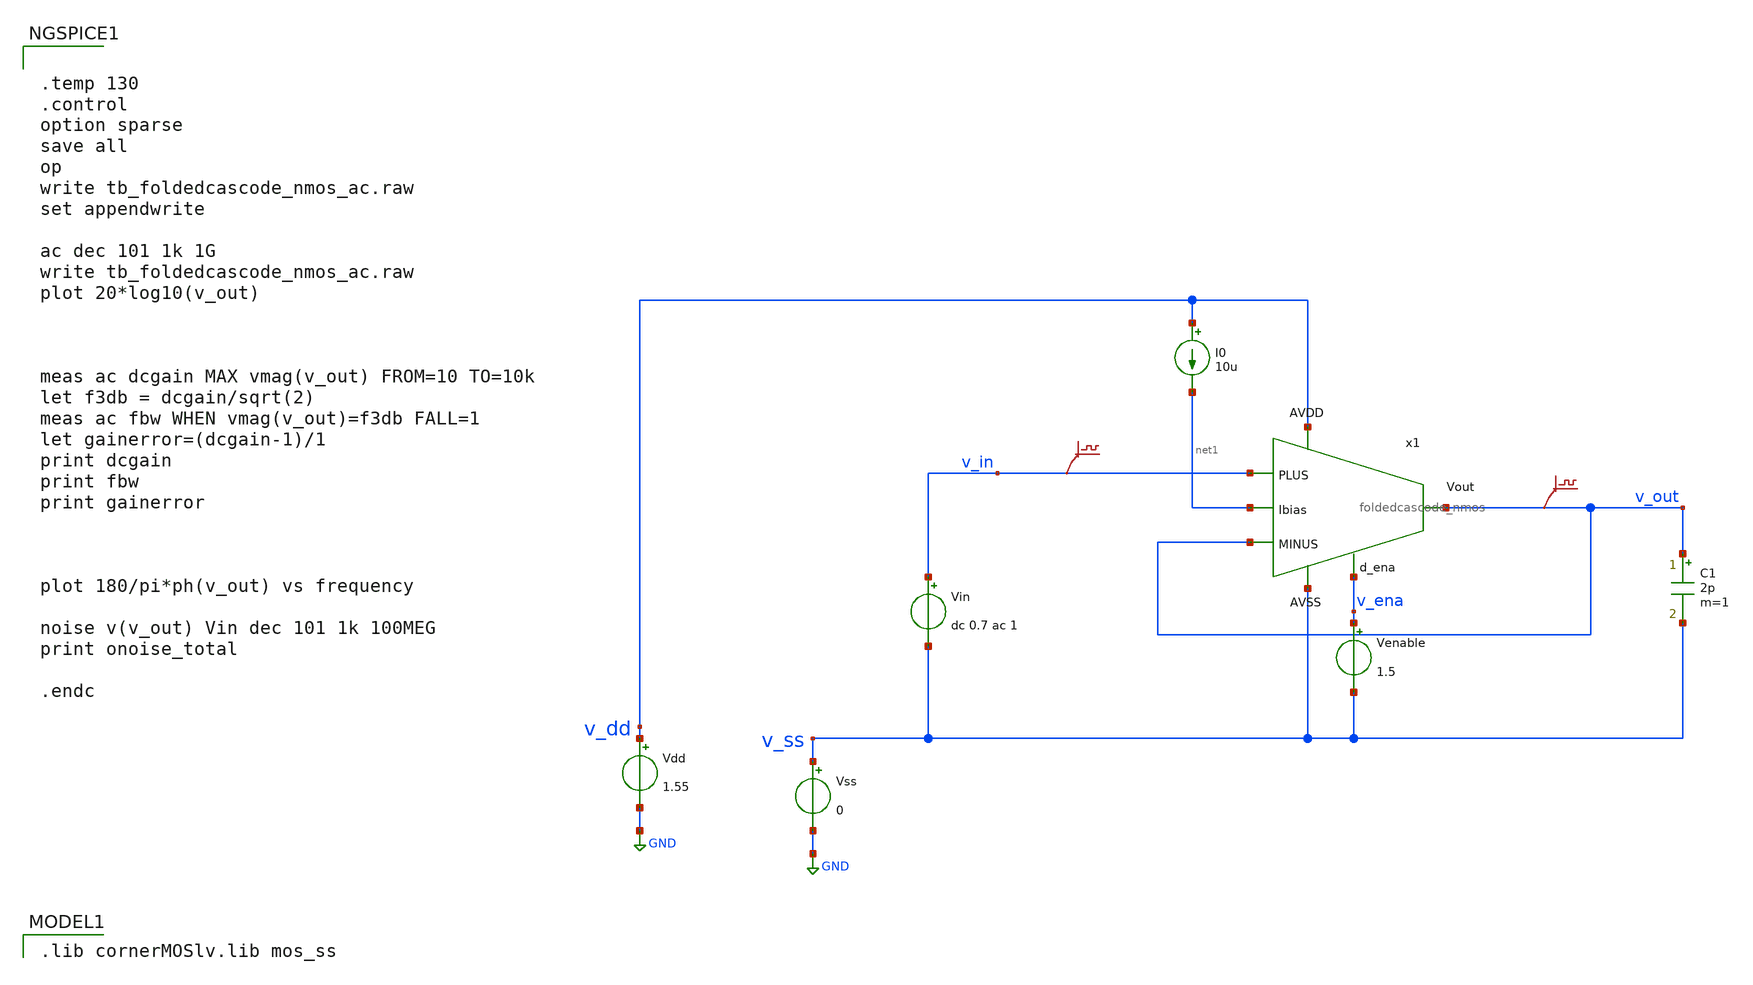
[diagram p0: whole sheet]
** sch_path: Designs/otas/tb_foldedcascode_nmos_ac.sch
* (c) 2025 Thesis_HP, Apache-2.0 license
**.subckt tb_foldedcascode_nmos_ac
Vss v_ss GND 0
Vdd v_dd GND 1.55
Vin v_in v_ss dc 0.7 ac 1
.save v(v_in)
I0 v_dd net1 10u
C1 v_out v_ss 2p m=1
.save v(v_out)
Venable v_ena v_ss 1.5
x1 v_dd v_in v_out v_out net1 v_ena v_ss foldedcascode_nmos
**** begin user architecture code
 .lib cornerMOSlv.lib mos_ss



.temp 130
.control
option sparse
save all
op
write tb_foldedcascode_nmos_ac.raw
set appendwrite

ac dec 101 1k 1G
write tb_foldedcascode_nmos_ac.raw
plot 20*log10(v_out)



meas ac dcgain MAX vmag(v_out) FROM=10 TO=10k
let f3db = dcgain/sqrt(2)
meas ac fbw WHEN vmag(v_out)=f3db FALL=1
let gainerror=(dcgain-1)/1
print dcgain
print fbw
print gainerror



plot 180/pi*ph(v_out) vs frequency

noise v(v_out) Vin dec 101 1k 100MEG
print onoise_total

.endc


**** end user architecture code
**.ends

* expanding   symbol:  foldedcascode_nmos.sym # of pins=7
** sym_path: Designs/otas/foldedcascode_nmos.sym
** sch_path: Designs/otas/foldedcascode_nmos.sch
.subckt foldedcascode_nmos AVDD PLUS MINUS Vout Ibias d_ena AVSS
*.ipin PLUS
*.ipin MINUS
*.opin Vout
*.ipin AVDD
*.ipin AVSS
*.ipin Ibias
*.ipin d_ena
XM1 net5 PLUS net1 AVSS sg13_lv_nmos w=5u l=1u ng=1 m=1 mm_ok=1
XMt net11 Ibias AVSS AVSS sg13_lv_nmos w=5.5u l=5u ng=3 m=1 mm_ok=1
XM4 net3 net4 AVSS AVSS sg13_lv_nmos w=1u l=0.5u ng=1 m=1 mm_ok=1
XM3 net2 net4 AVSS AVSS sg13_lv_nmos w=1u l=0.5u ng=1 m=1 mm_ok=1
XM2 net6 MINUS net1 AVSS sg13_lv_nmos w=5u l=1u ng=1 m=1 mm_ok=1
XM7 net4 net9 net2 AVSS sg13_lv_nmos w=1.5u l=0.5u ng=1 m=1 mm_ok=1
XM8 Vout net9 net3 AVSS sg13_lv_nmos w=1.5u l=0.5u ng=1 m=1 mm_ok=1
XM5 net4 net8 net5 AVDD sg13_lv_pmos w=6u l=0.5u ng=1 m=1 mm_ok=1
XM9 net5 net7 AVDD AVDD sg13_lv_pmos w=6u l=0.5u ng=1 m=1 mm_ok=1
XM6 Vout net8 net6 AVDD sg13_lv_pmos w=6u l=0.5u ng=1 m=1 mm_ok=1
XM0 net6 net7 AVDD AVDD sg13_lv_pmos w=6u l=0.5u ng=1 m=1 mm_ok=1
XMb Ibias Ibias AVSS AVSS sg13_lv_nmos w=4u l=5u ng=2 m=1 mm_ok=1
XM11 net8 net8 net7 AVDD sg13_lv_pmos w=6u l=0.5u ng=2 m=1 mm_ok=1
XM12 net7 net7 AVDD AVDD sg13_lv_pmos w=6u l=0.5u ng=2 m=1 mm_ok=1
XM13 net12 net7 AVDD AVDD sg13_lv_pmos w=6u l=0.5u ng=2 m=1 mm_ok=1
XM14 net9 net9 AVSS AVSS sg13_lv_nmos w=1.5u l=0.5u ng=1 m=1 mm_ok=1
XMb1 net10 Ibias AVSS AVSS sg13_lv_nmos w=4u l=5u ng=2 m=1 mm_ok=1
Vmeas net8 net10 0
.save i(vmeas)
Vmeas1 net1 net11 0
.save i(vmeas1)
Vmeas2 net12 net9 0
.save i(vmeas2)
XMdecoup1 AVSS Ibias AVSS AVSS sg13_lv_nmos w=8u l=1u ng=4 m=1 mm_ok=1
XMdecoup2 AVSS net9 AVSS AVSS sg13_lv_nmos w=8u l=1u ng=4 m=1 mm_ok=1
XMdecoup3 AVDD net7 AVDD AVDD sg13_lv_pmos w=12u l=0.5u ng=4 m=1 mm_ok=1
XMdecoup4 AVDD net8 AVDD AVDD sg13_lv_pmos w=12u l=0.5u ng=4 m=1 mm_ok=1
XMpd3 ena ena_n AVSS AVSS sg13_lv_nmos w=1u l=0.13u ng=1 m=1 mm_ok=1
XMpd4 ena ena_n AVDD AVDD sg13_lv_pmos w=1u l=0.13u ng=1 m=1 mm_ok=1
XMpd1 ena_n d_ena AVSS AVSS sg13_lv_nmos w=1u l=0.13u ng=1 m=1 mm_ok=1
XMpd2 ena_n d_ena AVDD AVDD sg13_lv_pmos w=1u l=0.13u ng=1 m=1 mm_ok=1
XMpd5 Ibias ena_n AVSS AVSS sg13_lv_nmos w=1u l=0.13u ng=1 m=1 mm_ok=1
XMpd6 Ibias ena Ibias AVSS sg13_lv_nmos w=1u l=0.13u ng=1 m=1 mm_ok=1
XMpd7 net7 ena AVDD AVDD sg13_lv_pmos w=1u l=0.13u ng=1 m=1 mm_ok=1
XMpd8 net8 ena AVDD AVDD sg13_lv_pmos w=1u l=0.13u ng=1 m=1 mm_ok=1
XMpd9 net4 ena_n AVSS AVSS sg13_lv_nmos w=1u l=0.13u ng=1 m=1 mm_ok=1
XMpd10 net9 ena_n AVSS AVSS sg13_lv_nmos w=1u l=0.13u ng=1 m=1 mm_ok=1
XMpd11 Vout ena_n AVSS AVSS sg13_lv_nmos w=1u l=0.13u ng=1 m=1 mm_ok=1
.ends

.GLOBAL GND
.end
